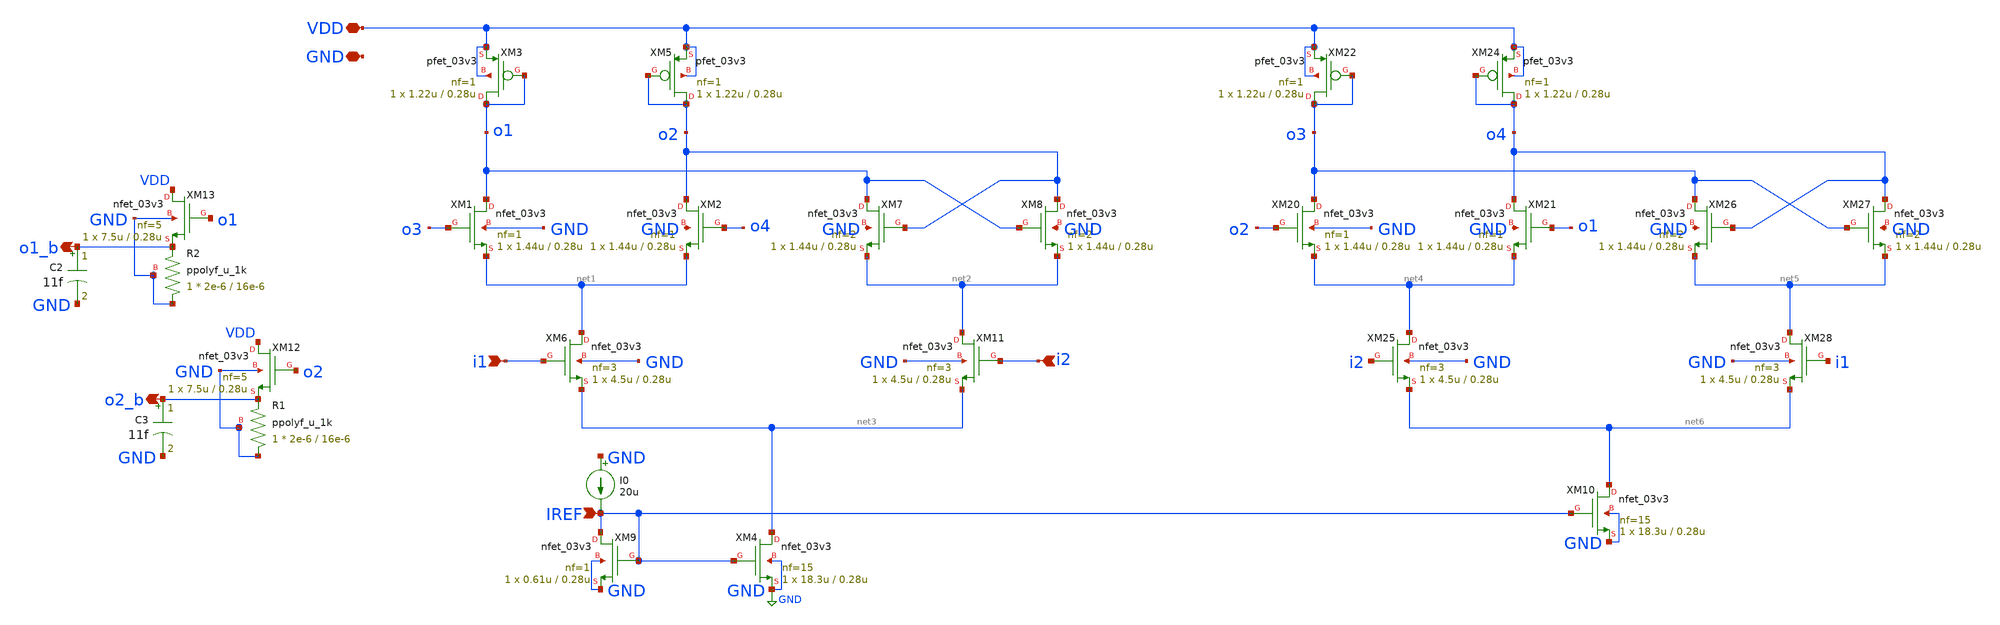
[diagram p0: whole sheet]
** sch_path: blocks/pll/cml_div.sch
**.subckt cml_div i2 i1 o2_b o1_b VDD GND IREF
*.ipin i2
*.ipin i1
*.opin o2_b
*.opin o1_b
*.iopin VDD
*.iopin GND
*.ipin IREF
XM1 o1 o3 net1 GND nfet_03v3 L=0.28u W=1.44u nf=1 ad='int((nf+1)/2) * W/nf * 0.18u' as='int((nf+2)/2) * W/nf * 0.18u'
+ pd='2*int((nf+1)/2) * (W/nf + 0.18u)' ps='2*int((nf+2)/2) * (W/nf + 0.18u)' nrd='0.18u / W' nrs='0.18u / W'
+ sa=0 sb=0 sd=0 m=1
XM2 o2 o4 net1 GND nfet_03v3 L=0.28u W=1.44u nf=1 ad='int((nf+1)/2) * W/nf * 0.18u' as='int((nf+2)/2) * W/nf * 0.18u'
+ pd='2*int((nf+1)/2) * (W/nf + 0.18u)' ps='2*int((nf+2)/2) * (W/nf + 0.18u)' nrd='0.18u / W' nrs='0.18u / W'
+ sa=0 sb=0 sd=0 m=1
XM3 o1 o1 VDD VDD pfet_03v3 L=0.28u W=1.22u nf=1 ad='int((nf+1)/2) * W/nf * 0.18u' as='int((nf+2)/2) * W/nf * 0.18u'
+ pd='2*int((nf+1)/2) * (W/nf + 0.18u)' ps='2*int((nf+2)/2) * (W/nf + 0.18u)' nrd='0.18u / W' nrs='0.18u / W'
+ sa=0 sb=0 sd=0 m=1
XM4 net3 IREF GND GND nfet_03v3 L=0.28u W=18.3u nf=15 ad='int((nf+1)/2) * W/nf * 0.18u' as='int((nf+2)/2) * W/nf * 0.18u'
+ pd='2*int((nf+1)/2) * (W/nf + 0.18u)' ps='2*int((nf+2)/2) * (W/nf + 0.18u)' nrd='0.18u / W' nrs='0.18u / W'
+ sa=0 sb=0 sd=0 m=1
XM5 o2 o2 VDD VDD pfet_03v3 L=0.28u W=1.22u nf=1 ad='int((nf+1)/2) * W/nf * 0.18u' as='int((nf+2)/2) * W/nf * 0.18u'
+ pd='2*int((nf+1)/2) * (W/nf + 0.18u)' ps='2*int((nf+2)/2) * (W/nf + 0.18u)' nrd='0.18u / W' nrs='0.18u / W'
+ sa=0 sb=0 sd=0 m=1
XM6 net1 i1 net3 GND nfet_03v3 L=0.28u W=4.5u nf=3 ad='int((nf+1)/2) * W/nf * 0.18u' as='int((nf+2)/2) * W/nf * 0.18u'
+ pd='2*int((nf+1)/2) * (W/nf + 0.18u)' ps='2*int((nf+2)/2) * (W/nf + 0.18u)' nrd='0.18u / W' nrs='0.18u / W'
+ sa=0 sb=0 sd=0 m=1
XM7 o1 o2 net2 GND nfet_03v3 L=0.28u W=1.44u nf=2 ad='int((nf+1)/2) * W/nf * 0.18u' as='int((nf+2)/2) * W/nf * 0.18u'
+ pd='2*int((nf+1)/2) * (W/nf + 0.18u)' ps='2*int((nf+2)/2) * (W/nf + 0.18u)' nrd='0.18u / W' nrs='0.18u / W'
+ sa=0 sb=0 sd=0 m=1
XM8 o2 o1 net2 GND nfet_03v3 L=0.28u W=1.44u nf=2 ad='int((nf+1)/2) * W/nf * 0.18u' as='int((nf+2)/2) * W/nf * 0.18u'
+ pd='2*int((nf+1)/2) * (W/nf + 0.18u)' ps='2*int((nf+2)/2) * (W/nf + 0.18u)' nrd='0.18u / W' nrs='0.18u / W'
+ sa=0 sb=0 sd=0 m=1
XM11 net2 i2 net3 GND nfet_03v3 L=0.28u W=4.5u nf=3 ad='int((nf+1)/2) * W/nf * 0.18u' as='int((nf+2)/2) * W/nf * 0.18u'
+ pd='2*int((nf+1)/2) * (W/nf + 0.18u)' ps='2*int((nf+2)/2) * (W/nf + 0.18u)' nrd='0.18u / W' nrs='0.18u / W'
+ sa=0 sb=0 sd=0 m=1
XM9 IREF IREF GND GND nfet_03v3 L=0.28u W=0.61u nf=1 ad='int((nf+1)/2) * W/nf * 0.18u' as='int((nf+2)/2) * W/nf * 0.18u'
+ pd='2*int((nf+1)/2) * (W/nf + 0.18u)' ps='2*int((nf+2)/2) * (W/nf + 0.18u)' nrd='0.18u / W' nrs='0.18u / W'
+ sa=0 sb=0 sd=0 m=1
XM20 o3 o2 net4 GND nfet_03v3 L=0.28u W=1.44u nf=1 ad='int((nf+1)/2) * W/nf * 0.18u' as='int((nf+2)/2) * W/nf * 0.18u'
+ pd='2*int((nf+1)/2) * (W/nf + 0.18u)' ps='2*int((nf+2)/2) * (W/nf + 0.18u)' nrd='0.18u / W' nrs='0.18u / W'
+ sa=0 sb=0 sd=0 m=1
XM21 o4 o1 net4 GND nfet_03v3 L=0.28u W=1.44u nf=1 ad='int((nf+1)/2) * W/nf * 0.18u' as='int((nf+2)/2) * W/nf * 0.18u'
+ pd='2*int((nf+1)/2) * (W/nf + 0.18u)' ps='2*int((nf+2)/2) * (W/nf + 0.18u)' nrd='0.18u / W' nrs='0.18u / W'
+ sa=0 sb=0 sd=0 m=1
XM22 o3 o3 VDD VDD pfet_03v3 L=0.28u W=1.22u nf=1 ad='int((nf+1)/2) * W/nf * 0.18u' as='int((nf+2)/2) * W/nf * 0.18u'
+ pd='2*int((nf+1)/2) * (W/nf + 0.18u)' ps='2*int((nf+2)/2) * (W/nf + 0.18u)' nrd='0.18u / W' nrs='0.18u / W'
+ sa=0 sb=0 sd=0 m=1
XM24 o4 o4 VDD VDD pfet_03v3 L=0.28u W=1.22u nf=1 ad='int((nf+1)/2) * W/nf * 0.18u' as='int((nf+2)/2) * W/nf * 0.18u'
+ pd='2*int((nf+1)/2) * (W/nf + 0.18u)' ps='2*int((nf+2)/2) * (W/nf + 0.18u)' nrd='0.18u / W' nrs='0.18u / W'
+ sa=0 sb=0 sd=0 m=1
XM25 net4 i2 net6 GND nfet_03v3 L=0.28u W=4.5u nf=3 ad='int((nf+1)/2) * W/nf * 0.18u' as='int((nf+2)/2) * W/nf * 0.18u'
+ pd='2*int((nf+1)/2) * (W/nf + 0.18u)' ps='2*int((nf+2)/2) * (W/nf + 0.18u)' nrd='0.18u / W' nrs='0.18u / W'
+ sa=0 sb=0 sd=0 m=1
XM26 o3 o4 net5 GND nfet_03v3 L=0.28u W=1.44u nf=2 ad='int((nf+1)/2) * W/nf * 0.18u' as='int((nf+2)/2) * W/nf * 0.18u'
+ pd='2*int((nf+1)/2) * (W/nf + 0.18u)' ps='2*int((nf+2)/2) * (W/nf + 0.18u)' nrd='0.18u / W' nrs='0.18u / W'
+ sa=0 sb=0 sd=0 m=1
XM27 o4 o3 net5 GND nfet_03v3 L=0.28u W=1.44u nf=2 ad='int((nf+1)/2) * W/nf * 0.18u' as='int((nf+2)/2) * W/nf * 0.18u'
+ pd='2*int((nf+1)/2) * (W/nf + 0.18u)' ps='2*int((nf+2)/2) * (W/nf + 0.18u)' nrd='0.18u / W' nrs='0.18u / W'
+ sa=0 sb=0 sd=0 m=1
XM28 net5 i1 net6 GND nfet_03v3 L=0.28u W=4.5u nf=3 ad='int((nf+1)/2) * W/nf * 0.18u' as='int((nf+2)/2) * W/nf * 0.18u'
+ pd='2*int((nf+1)/2) * (W/nf + 0.18u)' ps='2*int((nf+2)/2) * (W/nf + 0.18u)' nrd='0.18u / W' nrs='0.18u / W'
+ sa=0 sb=0 sd=0 m=1
XM10 net6 IREF GND GND nfet_03v3 L=0.28u W=18.3u nf=15 ad='int((nf+1)/2) * W/nf * 0.18u' as='int((nf+2)/2) * W/nf * 0.18u'
+ pd='2*int((nf+1)/2) * (W/nf + 0.18u)' ps='2*int((nf+2)/2) * (W/nf + 0.18u)' nrd='0.18u / W' nrs='0.18u / W'
+ sa=0 sb=0 sd=0 m=1
I0 GND IREF 20u
C2 o1_b GND 11f m=1
XM12 VDD o2 o2_b GND nfet_03v3 L=0.28u W=7.5u nf=5 ad='int((nf+1)/2) * W/nf * 0.18u' as='int((nf+2)/2) * W/nf * 0.18u'
+ pd='2*int((nf+1)/2) * (W/nf + 0.18u)' ps='2*int((nf+2)/2) * (W/nf + 0.18u)' nrd='0.18u / W' nrs='0.18u / W'
+ sa=0 sb=0 sd=0 m=1
XR1 GND o2_b GND ppolyf_u_1k r_width=2e-6 r_length=16e-6 m=1
XM13 VDD o1 o1_b GND nfet_03v3 L=0.28u W=7.5u nf=5 ad='int((nf+1)/2) * W/nf * 0.18u' as='int((nf+2)/2) * W/nf * 0.18u'
+ pd='2*int((nf+1)/2) * (W/nf + 0.18u)' ps='2*int((nf+2)/2) * (W/nf + 0.18u)' nrd='0.18u / W' nrs='0.18u / W'
+ sa=0 sb=0 sd=0 m=1
XR2 GND o1_b GND ppolyf_u_1k r_width=2e-6 r_length=16e-6 m=1
C3 o2_b GND 11f m=1
**** begin user architecture code

.include $::180MCU_MODELS/design.ngspice
.lib $::180MCU_MODELS/sm141064.ngspice typical
.lib $::180MCU_MODELS/sm141064.ngspice res_typical


V_VDD   VDD     0 DC 3.3
*V_VinP   i1     0 PULSE(0.4 1.3 0 52p 90p 53p 200p)
*V_VinN   i2     0 PULSE(1.3 0.4 0 52p 90p 53p 200p)
V_VinP   i1     0 SIN(0.85 0.45 2G 0 0 0)
V_VinN   i2     0 SIN(0.85 0.45 2G 0 0 180)

.control
save all
tran 10p 350n
write my_test_1.raw
.endc


**** end user architecture code
**.ends
.GLOBAL GND
.end
